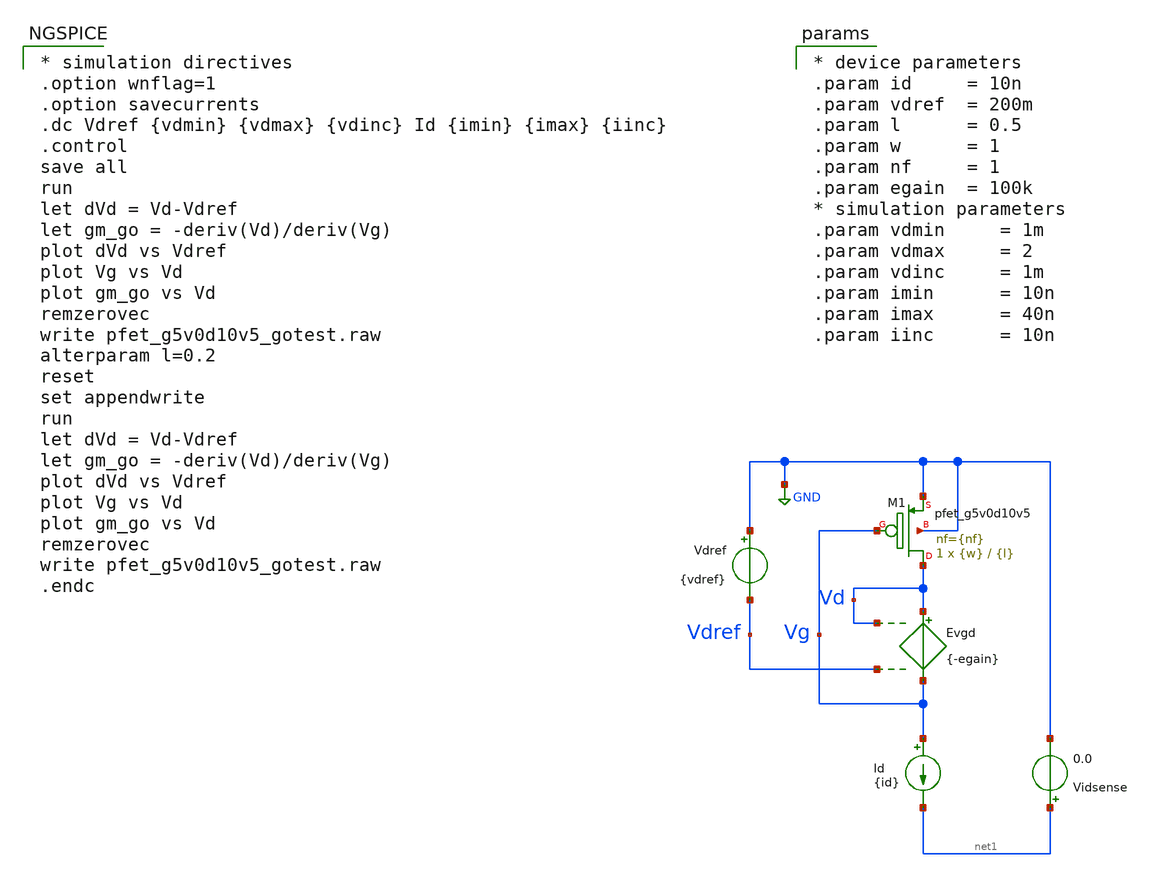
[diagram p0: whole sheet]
** sch_path: xschem/pfet_g5v0d10v5_gotest.sch
**.subckt pfet_g5v0d10v5_gotest
Evgd Vd Vg Vd Vdref {-egain}
Id Vg net1 {id}
Vdref GND Vdref {vdref}
Vidsense net1 GND 0.0
XM1 Vd Vg GND GND sky130_fd_pr__pfet_g5v0d10v5 L={l} W={w} nf={nf} ad='int(({nf} + 1)/2) * {w} / {nf} * 0.29'
+ as='int(({nf} + 2)/2) * {w} / {nf} * 0.29' pd='2*int(({nf} + 1)/2) * ({w} / {nf} + 0.29)' ps='2*int(({nf} + 2)/2) * ({w} / {nf} + 0.29)'
+ nrd='0.29 / {w} ' nrs='0.29 / {w} ' sa=0 sb=0 sd=0 mult=1 m=1
**** begin user architecture code

** opencircuitdesign pdks install
.lib $::SKYWATER_MODELS/sky130.lib.spice tt



* simulation directives
.option wnflag=1
.option savecurrents
.dc Vdref {vdmin} {vdmax} {vdinc} Id {imin} {imax} {iinc}
.control
save all
run
let dVd = Vd-Vdref
let gm_go = -deriv(Vd)/deriv(Vg)
plot dVd vs Vdref
plot Vg vs Vd
plot gm_go vs Vd
remzerovec
write pfet_g5v0d10v5_gotest.raw
alterparam l=0.2
reset
set appendwrite
run
let dVd = Vd-Vdref
let gm_go = -deriv(Vd)/deriv(Vg)
plot dVd vs Vdref
plot Vg vs Vd
plot gm_go vs Vd
remzerovec
write pfet_g5v0d10v5_gotest.raw
.endc



* device parameters
.param id     = 10n
.param vdref  = 200m
.param l      = 0.5
.param w      = 1
.param nf     = 1
.param egain  = 100k
* simulation parameters
.param vdmin     = 1m
.param vdmax     = 2
.param vdinc     = 1m
.param imin      = 10n
.param imax      = 40n
.param iinc      = 10n


**** end user architecture code
**.ends
.GLOBAL GND
.end
